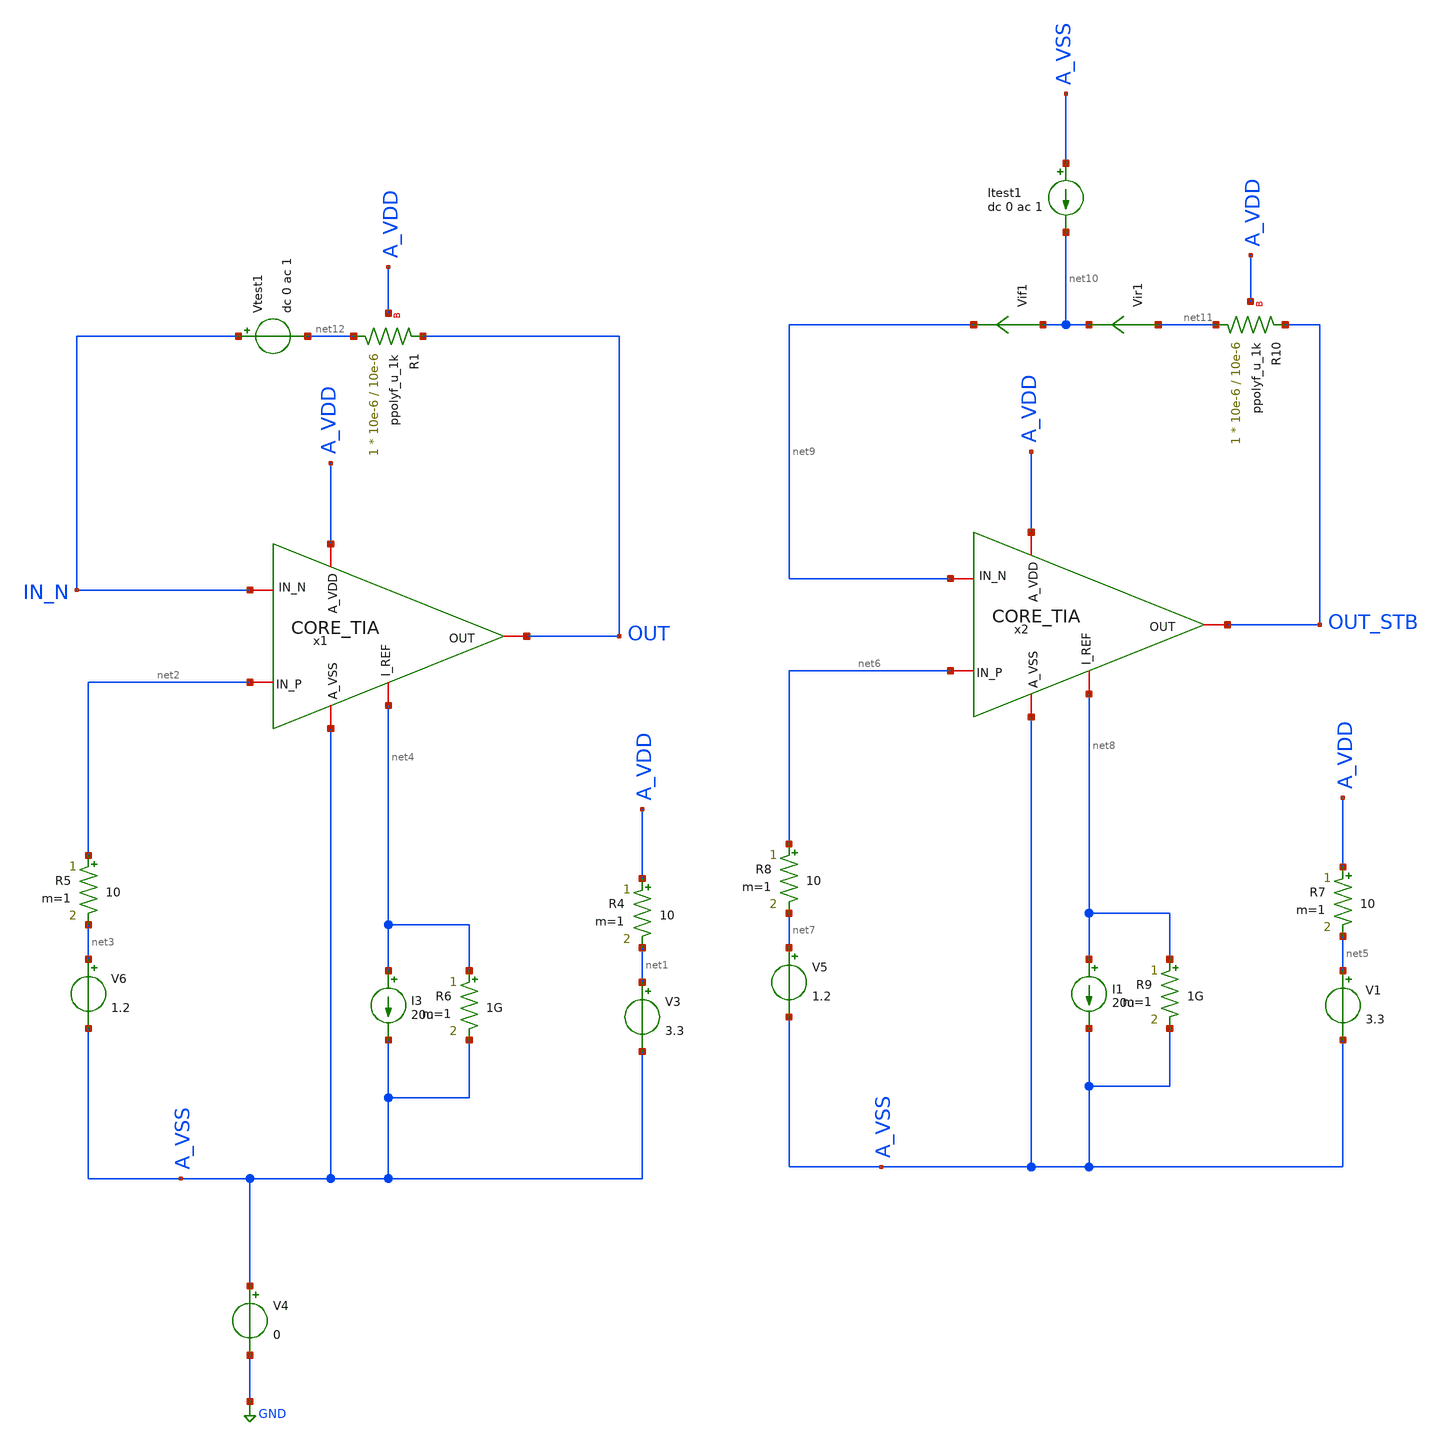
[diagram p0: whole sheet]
** sch_path: designs/libs/TIA/TB_CORE_STB.sch
**.subckt TB_CORE_STB
x1 A_VDD A_VSS IN_N net2 net4 OUT CORE_TIA
V3 net1 A_VSS 3.3
V4 A_VSS GND 0
V6 net3 A_VSS 1.2
I3 net4 A_VSS 20u
R4 A_VDD net1 10 m=1
R5 net2 net3 10 m=1
R6 net4 A_VSS 1G m=1
XR1 net12 OUT A_VDD ppolyf_u_1k r_width=10e-6 r_length=10e-6 m=1
Vtest1 IN_N net12 dc 0 ac 1
x2 A_VDD A_VSS net9 net6 net8 OUT_STB CORE_TIA
V1 net5 A_VSS 3.3
V5 net7 A_VSS 1.2
I1 net8 A_VSS 20u
R7 A_VDD net5 10 m=1
R8 net6 net7 10 m=1
R9 net8 A_VSS 1G m=1
XR10 net11 OUT_STB A_VDD ppolyf_u_1k r_width=10e-6 r_length=10e-6 m=1
Vir1 net11 net10 0
.save i(vir1)
Vif1 net10 net9 0
.save i(vif1)
Itest1 A_VSS net10 dc 0 ac 1
**** begin user architecture code

.include $::180MCU_MODELS/design.ngspice
.lib $::180MCU_MODELS/sm141064.ngspice typical
.lib $::180MCU_MODELS/sm141064.ngspice res_typical
.lib $::180MCU_MODELS/sm141064.ngspice mimcap_typical
.lib $::180MCU_MODELS/sm141064.ngspice cap_mim




.control
save all


** Simulation
op
ac dec 1001 1 1G
**remzerovec

**set appendwrite

* Middlebrook's Method
let tv=-v(OUT)/v(IN_N)
let ti=-i(vir1)/i(vif1)
let tmb=(tv*ti - 1)/(tv + ti + 2)


let mag = db(tmb)

let phase = 180/pi*cphase(tmb)




** Plots

plot mag ylabel 'Magnitude - Middlebrook'
plot phase ylabel 'Phase - Middlebrook'


setplot ac1

write TB_CORE_STB.raw
.endc


**** end user architecture code
**.ends
.GLOBAL GND
.end
